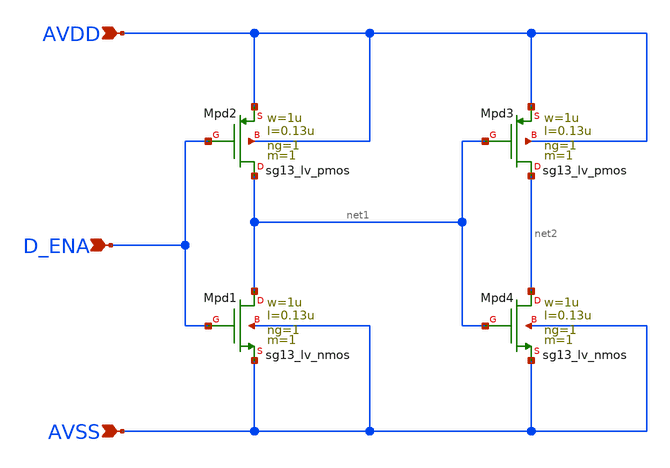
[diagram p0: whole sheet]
** sch_path: Designs/otas/1_schematics/enable_pins.sch
**.subckt enable_pins AVSS AVDD D_ENA
*.ipin AVSS
*.ipin AVDD
*.ipin D_ENA
XMpd2 net1 D_ENA AVDD AVDD sg13_lv_pmos w=1u l=0.13u ng=1 m=1 mm_ok=1
XMpd3 net2 net1 AVDD AVDD sg13_lv_pmos w=1u l=0.13u ng=1 m=1 mm_ok=1
XMpd1 net1 D_ENA AVSS AVSS sg13_lv_nmos w=1u l=0.13u ng=1 m=1 mm_ok=1
XMpd4 net2 net1 AVSS AVSS sg13_lv_nmos w=1u l=0.13u ng=1 m=1 mm_ok=1
**.ends
.end
